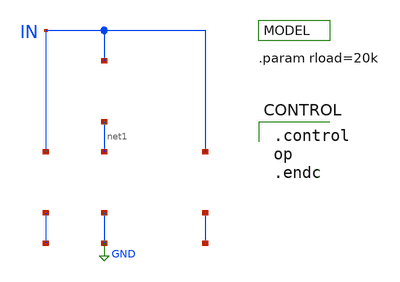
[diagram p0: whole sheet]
** sch_path: tests/data/schem/devlib/tb/ihp_style_tb.sch
* SPDX-License-Identifier: Apache-2.0
* Copyright 2026 The Hefesto Authors
**.subckt ihp_style_tb
Vin IN GND 1.2
Vmeas IN net1 0 .save I( Vmeas )
R1 net1 GND 10k m=1
C1 IN GND 1p m=1
**** begin user architecture code

.param rload=20k


.control
op
.endc

**** end user architecture code
**.ends
.GLOBAL GND
.end
